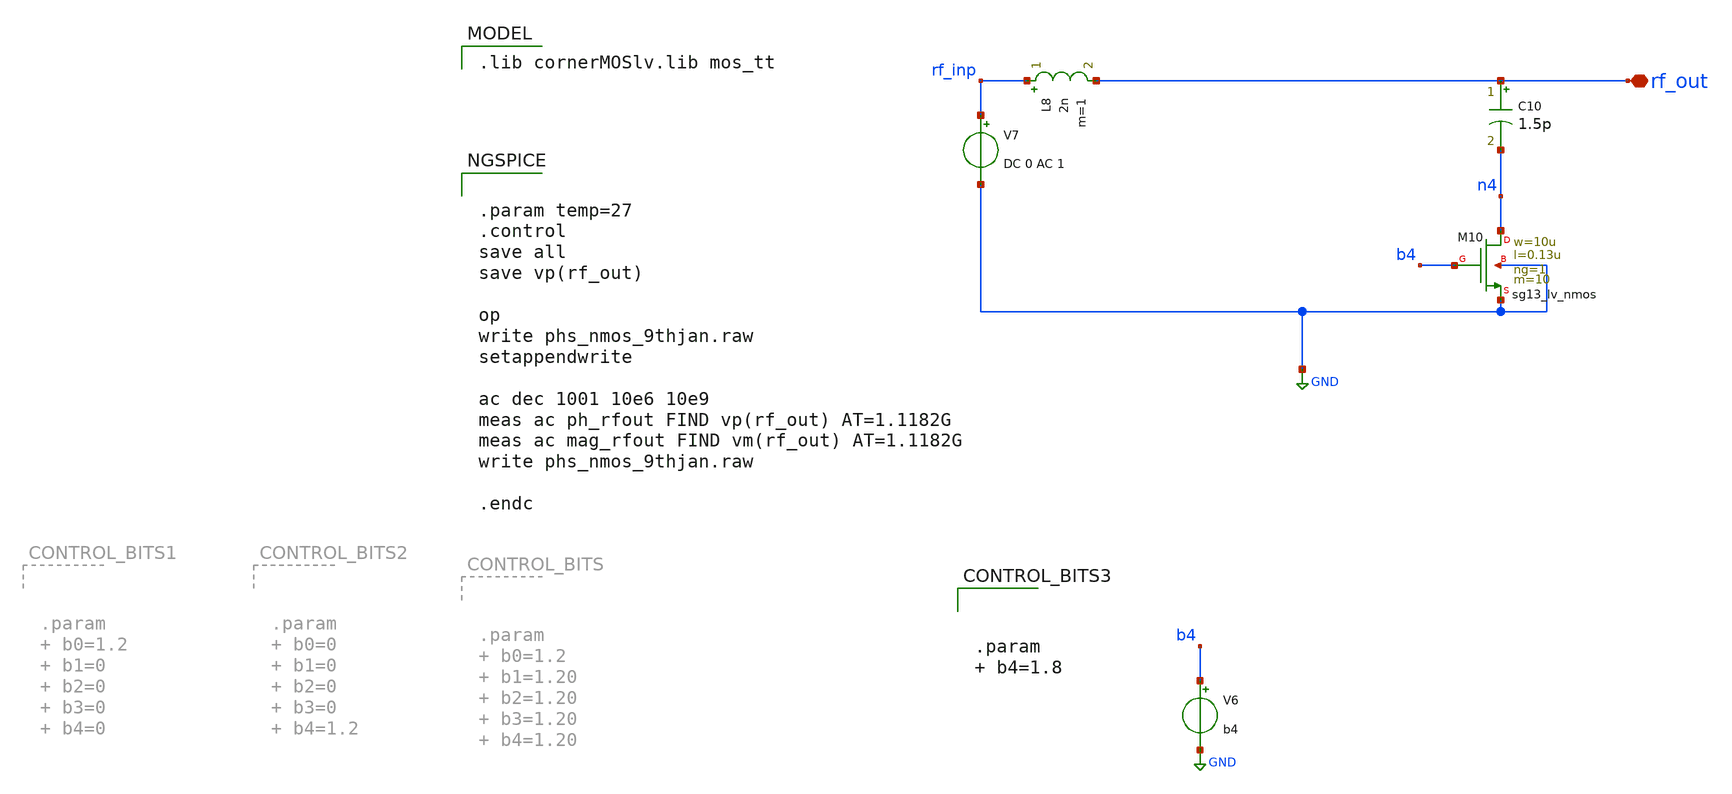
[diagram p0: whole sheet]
** sch_path: xschem/phs_nmos_9thjan.sch
**.subckt phs_nmos_9thjan rf_out
*.iopin rf_out
V6 b4 GND b4
L8 rf_inp rf_out 2n m=1
C10 rf_out n4 1.5p m=1
V7 rf_inp GND DC 0 AC 1
XM10 n4 b4 GND GND sg13_lv_nmos w=10u l=0.13u ng=1 m=10 mm_ok=1
**** begin user architecture code
 .lib cornerMOSlv.lib mos_tt



.param temp=27
.control
save all
save vp(rf_out)

op
write phs_nmos_9thjan.raw
setappendwrite

ac dec 1001 10e6 10e9
meas ac ph_rfout FIND vp(rf_out) AT=1.1182G
meas ac mag_rfout FIND vm(rf_out) AT=1.1182G
write phs_nmos_9thjan.raw

.endc





.param   b4=1.8


**** end user architecture code
**.ends
.GLOBAL GND
.end
